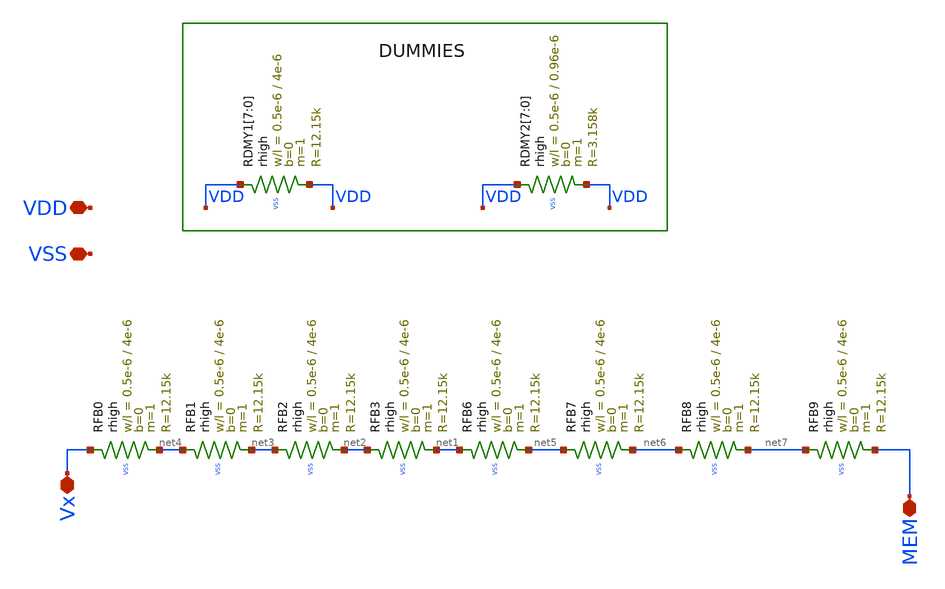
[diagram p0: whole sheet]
** sch_path: OSC9996-main/schematic/xschem/resistence_bank.sch
**.subckt resistence_bank VDD Vx MEM VSS
*.iopin VDD
*.iopin Vx
*.iopin MEM
*.iopin VSS
XRFB0 Vx net4 VSS rhigh w=0.5e-6 l=4e-6 m=1 b=0 mm_ok=1
XRFB1 net4 net3 VSS rhigh w=0.5e-6 l=4e-6 m=1 b=0 mm_ok=1
XRFB2 net3 net2 VSS rhigh w=0.5e-6 l=4e-6 m=1 b=0 mm_ok=1
XRFB3 net2 net1 VSS rhigh w=0.5e-6 l=4e-6 m=1 b=0 mm_ok=1
XRDMY1[7] VDD VDD VSS rhigh w=0.5e-6 l=4e-6 m=1 b=0 mm_ok=1
XRDMY1[6] VDD VDD VSS rhigh w=0.5e-6 l=4e-6 m=1 b=0 mm_ok=1
XRDMY1[5] VDD VDD VSS rhigh w=0.5e-6 l=4e-6 m=1 b=0 mm_ok=1
XRDMY1[4] VDD VDD VSS rhigh w=0.5e-6 l=4e-6 m=1 b=0 mm_ok=1
XRDMY1[3] VDD VDD VSS rhigh w=0.5e-6 l=4e-6 m=1 b=0 mm_ok=1
XRDMY1[2] VDD VDD VSS rhigh w=0.5e-6 l=4e-6 m=1 b=0 mm_ok=1
XRDMY1[1] VDD VDD VSS rhigh w=0.5e-6 l=4e-6 m=1 b=0 mm_ok=1
XRDMY1[0] VDD VDD VSS rhigh w=0.5e-6 l=4e-6 m=1 b=0 mm_ok=1
XRFB6 net1 net5 VSS rhigh w=0.5e-6 l=4e-6 m=1 b=0 mm_ok=1
XRFB7 net5 net6 VSS rhigh w=0.5e-6 l=4e-6 m=1 b=0 mm_ok=1
XRFB8 net6 net7 VSS rhigh w=0.5e-6 l=4e-6 m=1 b=0 mm_ok=1
XRFB9 net7 MEM VSS rhigh w=0.5e-6 l=4e-6 m=1 b=0 mm_ok=1
XRDMY2[7] VDD VDD VSS rhigh w=0.5e-6 l=0.96e-6 m=1 b=0 mm_ok=1
XRDMY2[6] VDD VDD VSS rhigh w=0.5e-6 l=0.96e-6 m=1 b=0 mm_ok=1
XRDMY2[5] VDD VDD VSS rhigh w=0.5e-6 l=0.96e-6 m=1 b=0 mm_ok=1
XRDMY2[4] VDD VDD VSS rhigh w=0.5e-6 l=0.96e-6 m=1 b=0 mm_ok=1
XRDMY2[3] VDD VDD VSS rhigh w=0.5e-6 l=0.96e-6 m=1 b=0 mm_ok=1
XRDMY2[2] VDD VDD VSS rhigh w=0.5e-6 l=0.96e-6 m=1 b=0 mm_ok=1
XRDMY2[1] VDD VDD VSS rhigh w=0.5e-6 l=0.96e-6 m=1 b=0 mm_ok=1
XRDMY2[0] VDD VDD VSS rhigh w=0.5e-6 l=0.96e-6 m=1 b=0 mm_ok=1
**.ends
.end
